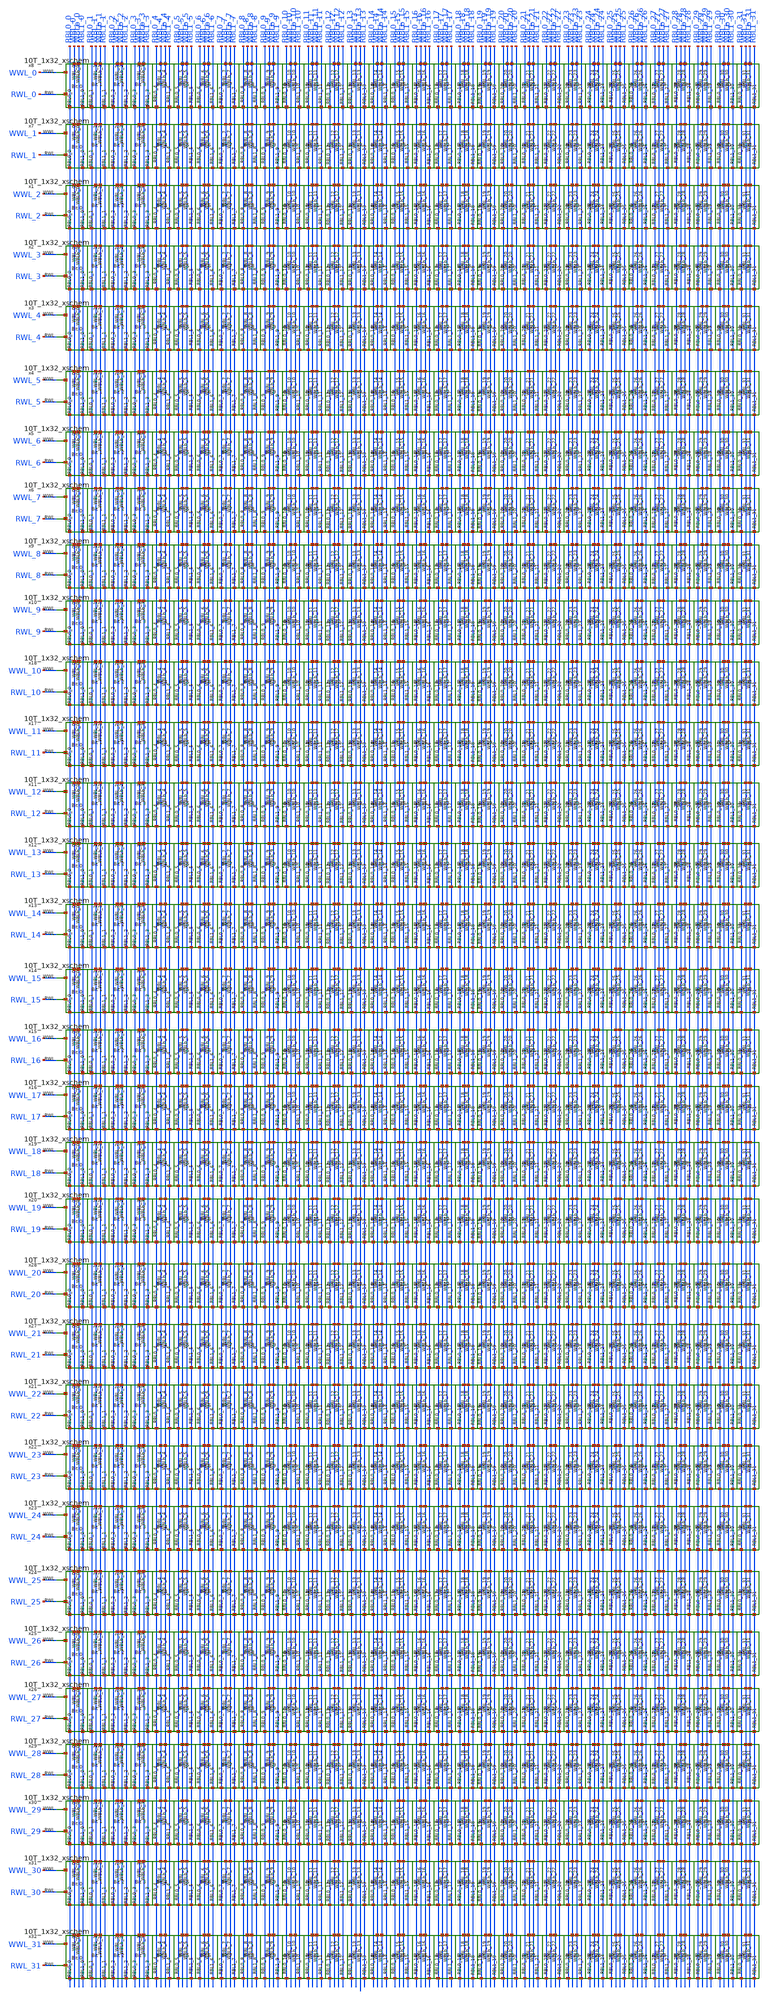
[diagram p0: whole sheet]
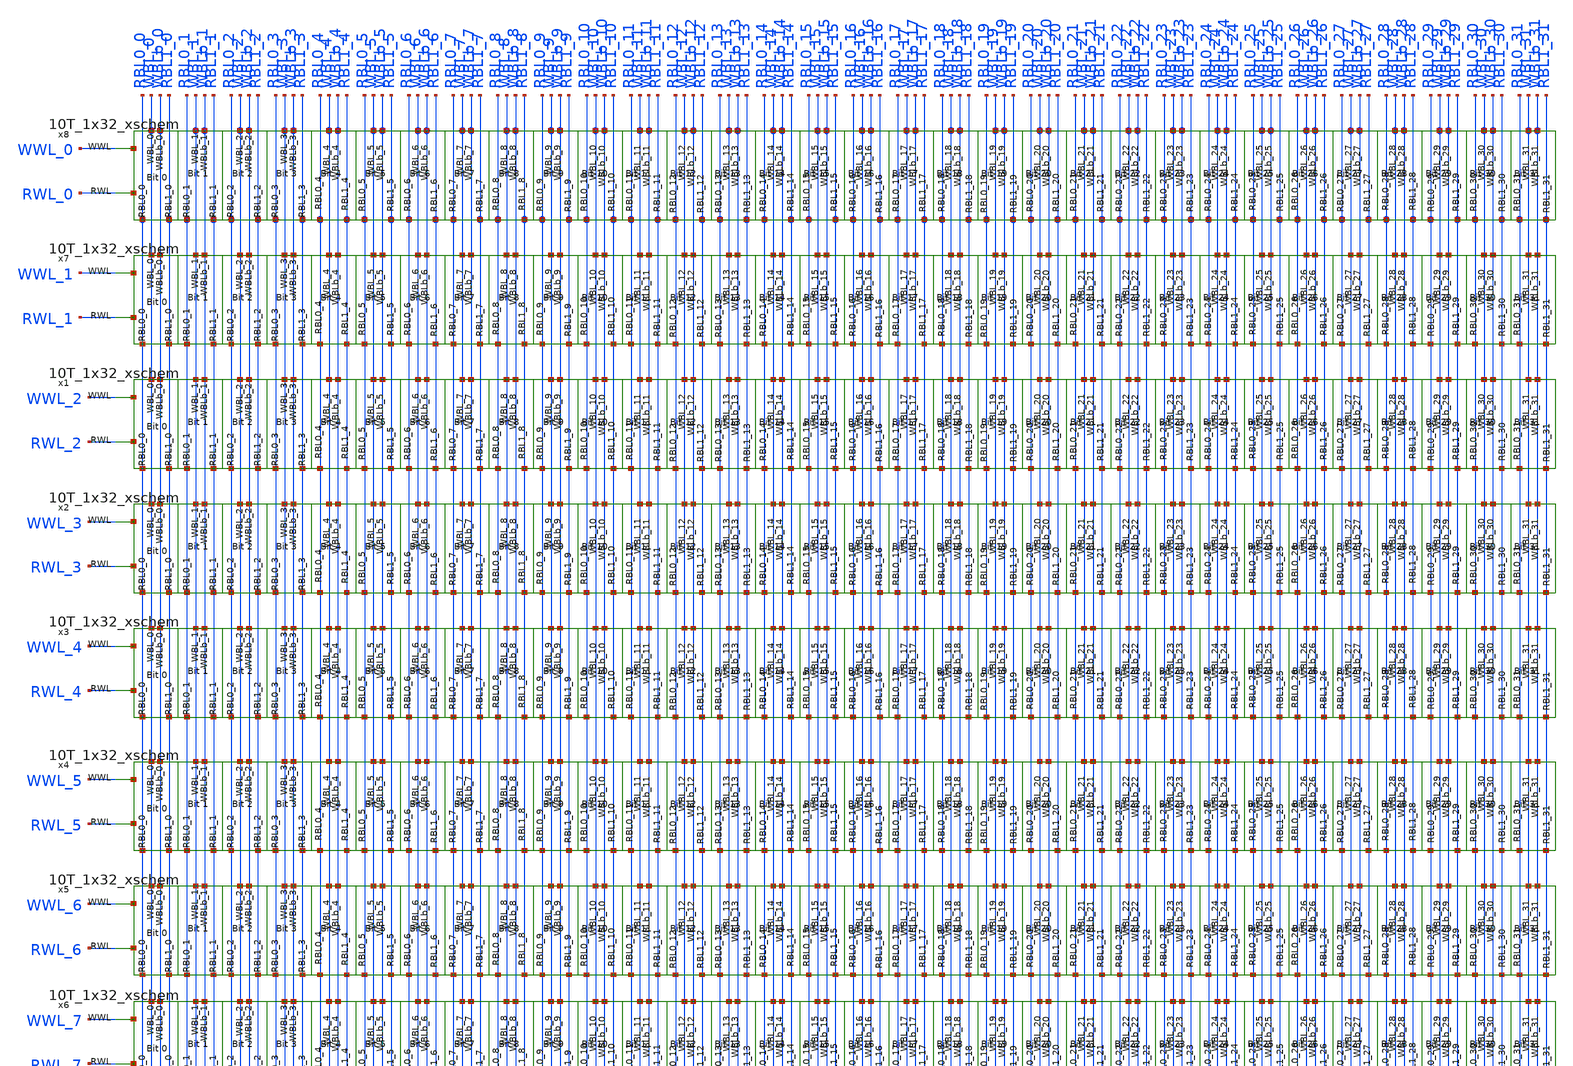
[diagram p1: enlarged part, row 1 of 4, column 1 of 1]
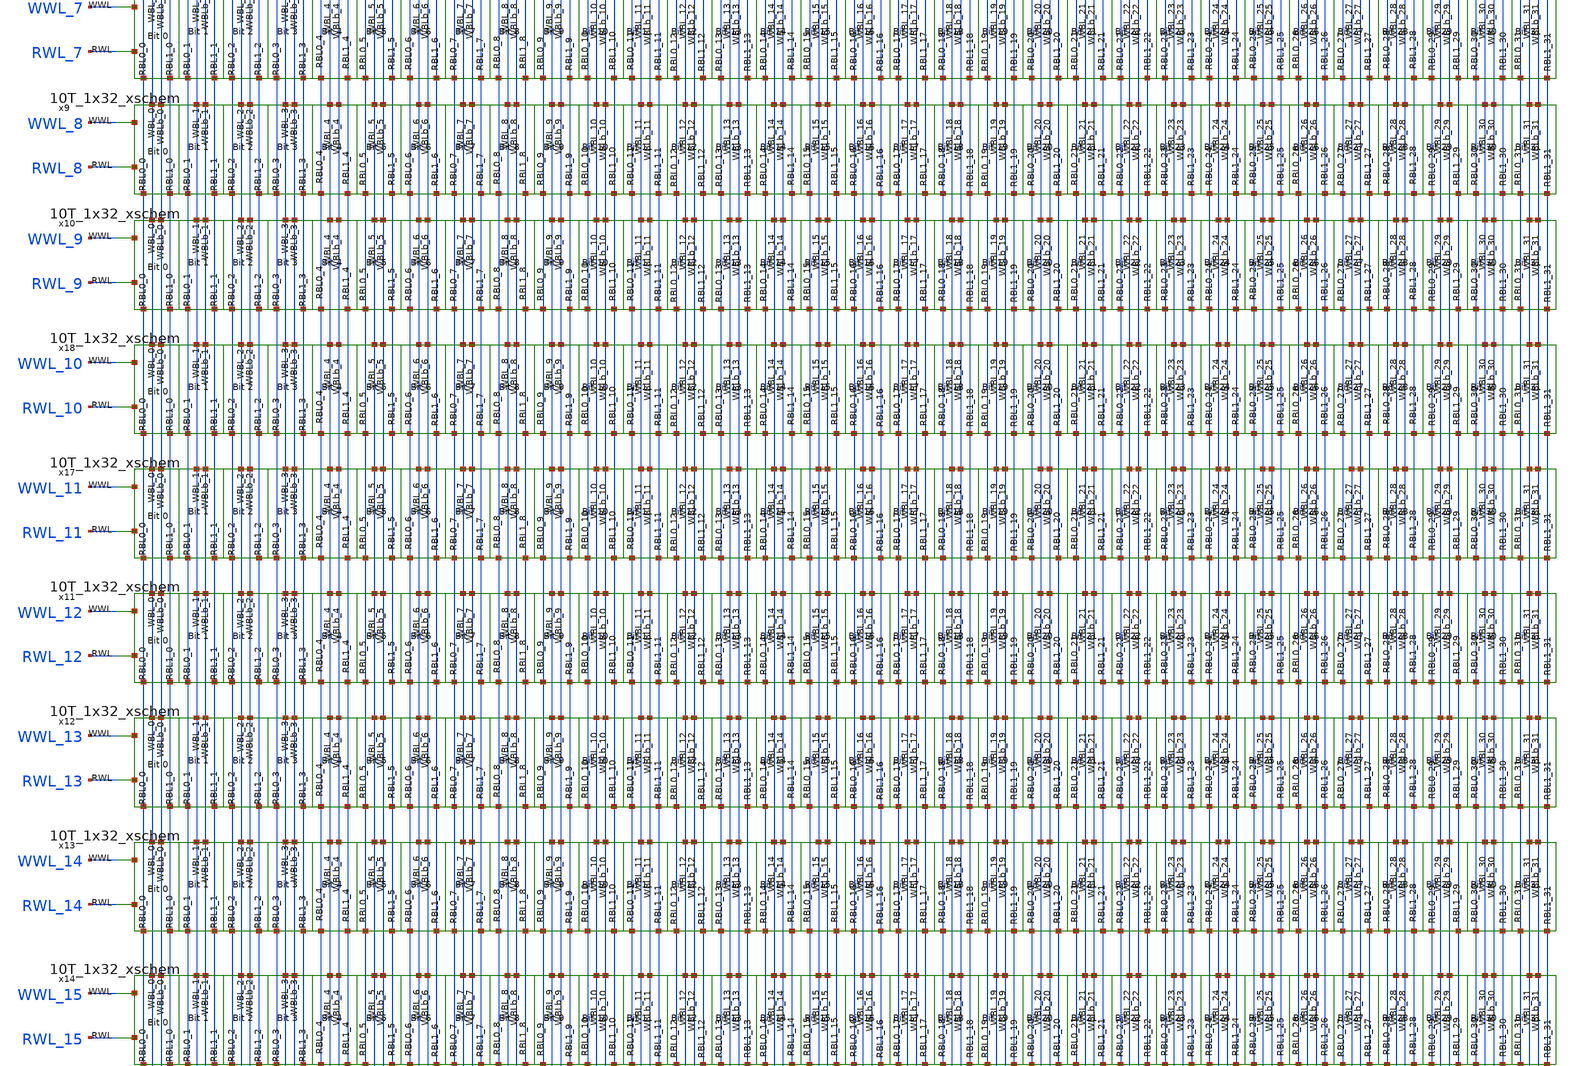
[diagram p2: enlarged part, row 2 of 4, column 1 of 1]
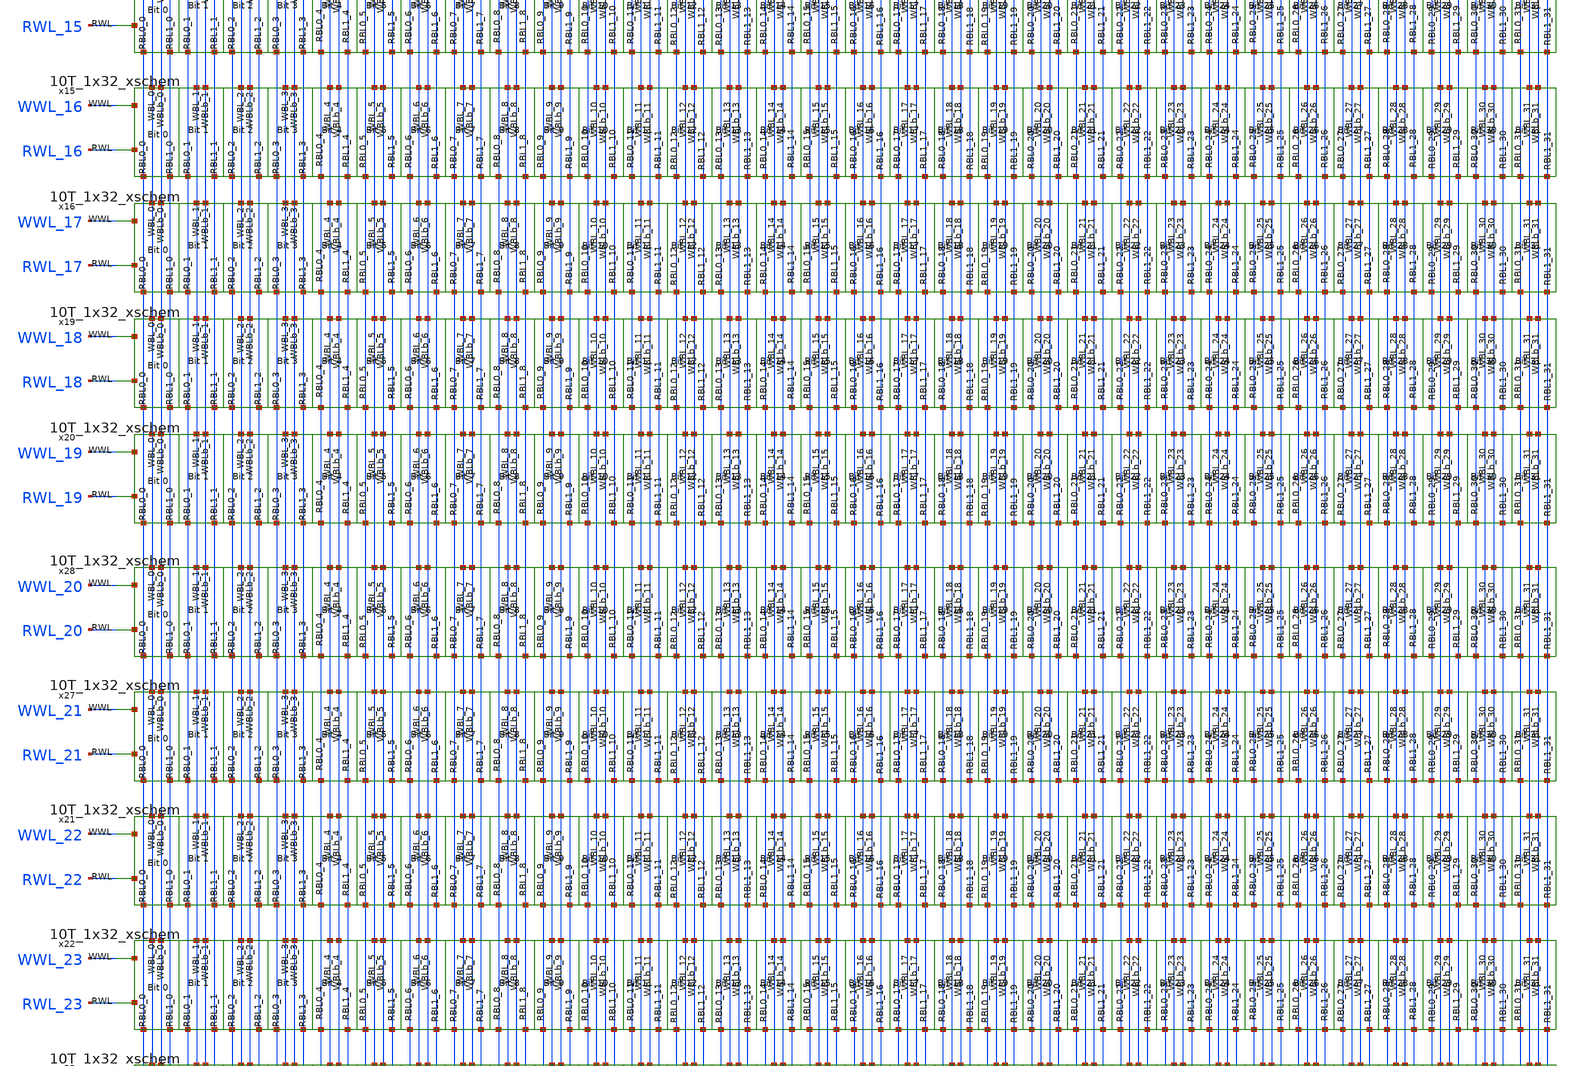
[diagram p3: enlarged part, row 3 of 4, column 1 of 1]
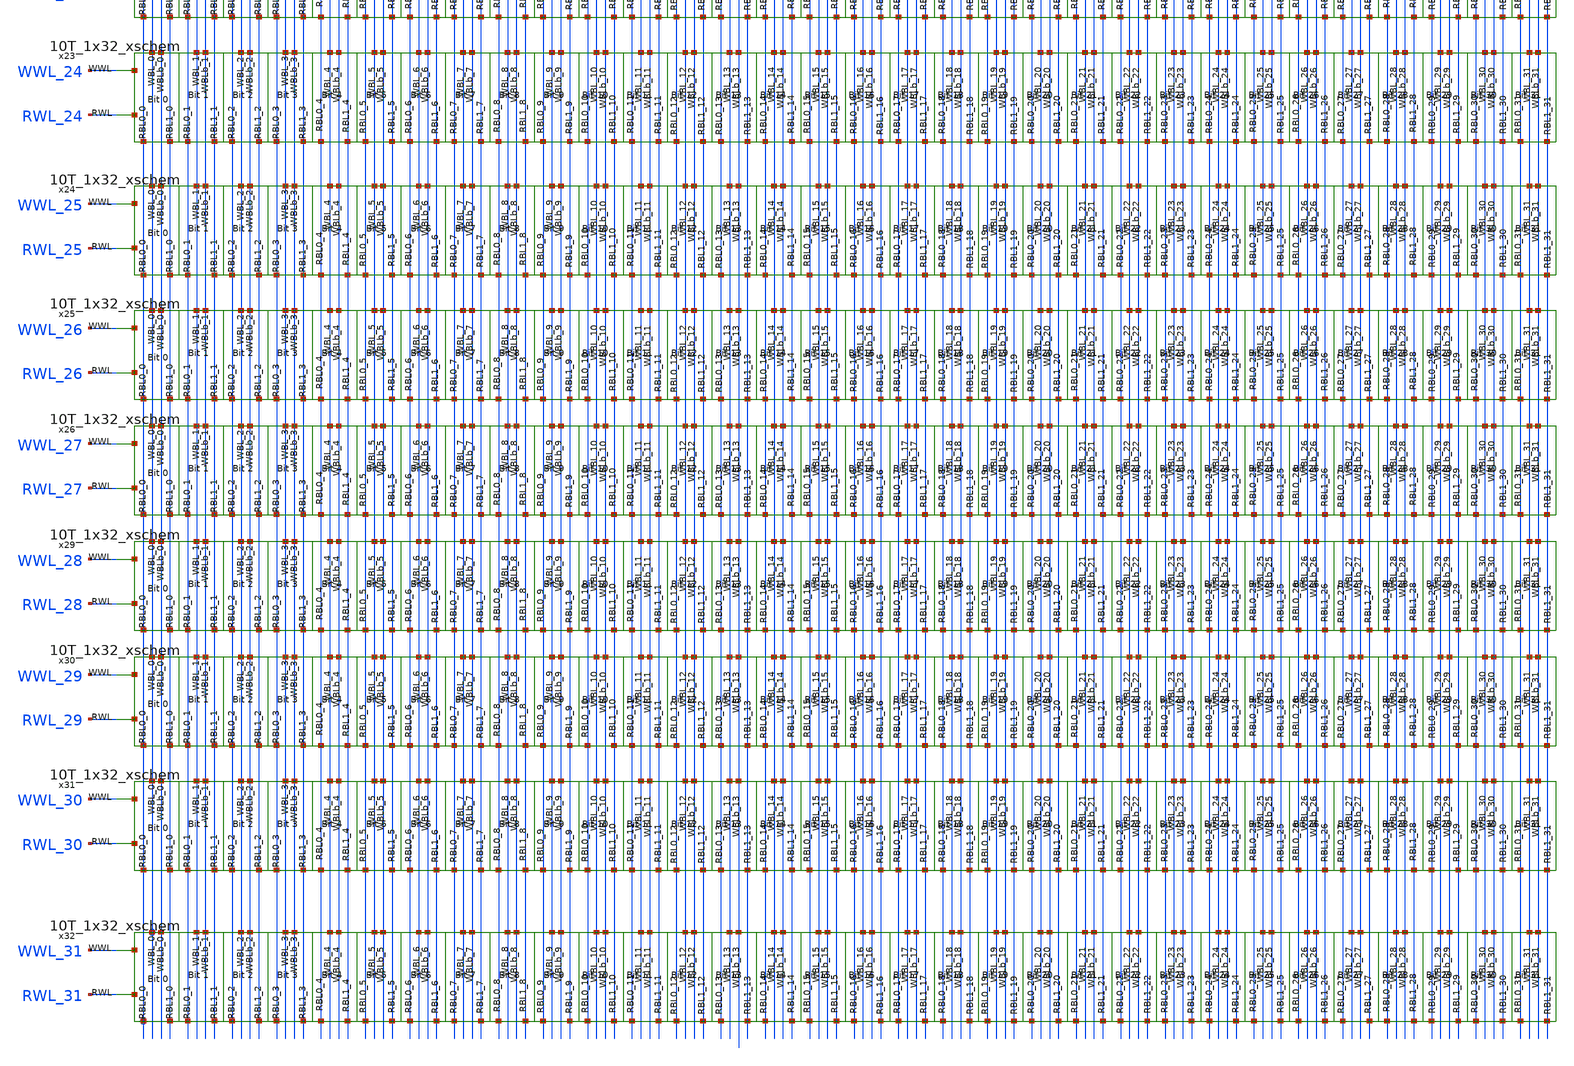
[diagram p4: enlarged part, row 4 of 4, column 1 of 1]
** sch_path: custom_layout/10T_32x32_xschem.sch
**.subckt 10T_32x32_xschem
x1 RBL0_22 WBL_25 RBL0_30 WBL_17 WBL_9 WBL_1 RBL0_14 RBL0_6 WBL_18 RBL0_18 RBL0_26 WBL_26 WBL_2
+ RBL0_2 RBL0_10 WBL_10 WBL_19 WBL_27 RBL1_30 RBL1_22 RBL1_14 WBL_3 RBL1_6 WBL_11 WBLb_30 WBLb_22 RBL0_31
+ RBL0_23 RBL0_7 RBL0_15 WBLb_6 WBLb_14 RBL1_21 WBL_20 RBL1_29 WBL_28 WBL_12 RBL1_13 RBL1_5 WBL_4 RBL1_20
+ WBL_23 WBL_31 RBL1_28 WBL_15 RBL1_4 RBL1_12 WBL_7 WBLb_29 WBLb_21 RBL1_19 RBL1_27 RBL1_3 WBLb_5 WBLb_13
+ RBL1_11 WBL_24 WBL_16 RBL1_18 RBL1_26 WBL_8 RBL1_2 RBL1_10 WBL_0 WBLb_26 RBL0_29 WBLb_18 RBL0_21 WBLb_10
+ RBL0_5 RBL0_13 WBLb_2 RBL1_25 WBLb_25 WBLb_17 RBL1_17 WBLb_9 RBL1_1 WBLb_1 RBL1_9 WBLb_24 WBLb_16 RBL1_23
+ RBL1_31 WBLb_0 WBLb_8 RBL1_7 RBL1_15 WBL_29 WBL_21 RBL0_17 RBL0_25 WBL_5 RBL0_1 WBL_13 RBL0_9 RBL0_28
+ WBLb_28 WBLb_20 RBL0_20 WBLb_12 WBLb_4 RBL0_4 RBL0_12 RBL0_27 WBL_30 WBL_22 RBL0_19 WBL_14 RBL0_11 WBL_6
+ RBL0_3 RBL1_24 WBLb_27 WBLb_19 RBL1_16 WBLb_11 RBL1_8 WBLb_3 RBL1_0 RBL0_24 WBLb_31 WBLb_23 RBL0_16 RBL0_8
+ WBLb_15 RBL0_0 WBLb_7 WWL_2 RWL_2 VDD GND 10T_1x32_xschem
x2 RBL0_22 WBL_25 RBL0_30 WBL_17 WBL_9 WBL_1 RBL0_14 RBL0_6 WBL_18 RBL0_18 RBL0_26 WBL_26 WBL_2
+ RBL0_2 RBL0_10 WBL_10 WBL_19 WBL_27 RBL1_30 RBL1_22 RBL1_14 WBL_3 RBL1_6 WBL_11 WBLb_30 WBLb_22 RBL0_31
+ RBL0_23 RBL0_7 RBL0_15 WBLb_6 WBLb_14 RBL1_21 WBL_20 RBL1_29 WBL_28 WBL_12 RBL1_13 RBL1_5 WBL_4 RBL1_20
+ WBL_23 WBL_31 RBL1_28 WBL_15 RBL1_4 RBL1_12 WBL_7 WBLb_29 WBLb_21 RBL1_19 RBL1_27 RBL1_3 WBLb_5 WBLb_13
+ RBL1_11 WBL_24 WBL_16 RBL1_18 RBL1_26 WBL_8 RBL1_2 RBL1_10 WBL_0 WBLb_26 RBL0_29 WBLb_18 RBL0_21 WBLb_10
+ RBL0_5 RBL0_13 WBLb_2 RBL1_25 WBLb_25 WBLb_17 RBL1_17 WBLb_9 RBL1_1 WBLb_1 RBL1_9 WBLb_24 WBLb_16 RBL1_23
+ RBL1_31 WBLb_0 WBLb_8 RBL1_7 RBL1_15 WBL_29 WBL_21 RBL0_17 RBL0_25 WBL_5 RBL0_1 WBL_13 RBL0_9 RBL0_28
+ WBLb_28 WBLb_20 RBL0_20 WBLb_12 WBLb_4 RBL0_4 RBL0_12 RBL0_27 WBL_30 WBL_22 RBL0_19 WBL_14 RBL0_11 WBL_6
+ RBL0_3 RBL1_24 WBLb_27 WBLb_19 RBL1_16 WBLb_11 RBL1_8 WBLb_3 RBL1_0 RBL0_24 WBLb_31 WBLb_23 RBL0_16 RBL0_8
+ WBLb_15 RBL0_0 WBLb_7 WWL_3 RWL_3 VDD GND 10T_1x32_xschem
x3 RBL0_22 WBL_25 RBL0_30 WBL_17 WBL_9 WBL_1 RBL0_14 RBL0_6 WBL_18 RBL0_18 RBL0_26 WBL_26 WBL_2
+ RBL0_2 RBL0_10 WBL_10 WBL_19 WBL_27 RBL1_30 RBL1_22 RBL1_14 WBL_3 RBL1_6 WBL_11 WBLb_30 WBLb_22 RBL0_31
+ RBL0_23 RBL0_7 RBL0_15 WBLb_6 WBLb_14 RBL1_21 WBL_20 RBL1_29 WBL_28 WBL_12 RBL1_13 RBL1_5 WBL_4 RBL1_20
+ WBL_23 WBL_31 RBL1_28 WBL_15 RBL1_4 RBL1_12 WBL_7 WBLb_29 WBLb_21 RBL1_19 RBL1_27 RBL1_3 WBLb_5 WBLb_13
+ RBL1_11 WBL_24 WBL_16 RBL1_18 RBL1_26 WBL_8 RBL1_2 RBL1_10 WBL_0 WBLb_26 RBL0_29 WBLb_18 RBL0_21 WBLb_10
+ RBL0_5 RBL0_13 WBLb_2 RBL1_25 WBLb_25 WBLb_17 RBL1_17 WBLb_9 RBL1_1 WBLb_1 RBL1_9 WBLb_24 WBLb_16 RBL1_23
+ RBL1_31 WBLb_0 WBLb_8 RBL1_7 RBL1_15 WBL_29 WBL_21 RBL0_17 RBL0_25 WBL_5 RBL0_1 WBL_13 RBL0_9 RBL0_28
+ WBLb_28 WBLb_20 RBL0_20 WBLb_12 WBLb_4 RBL0_4 RBL0_12 RBL0_27 WBL_30 WBL_22 RBL0_19 WBL_14 RBL0_11 WBL_6
+ RBL0_3 RBL1_24 WBLb_27 WBLb_19 RBL1_16 WBLb_11 RBL1_8 WBLb_3 RBL1_0 RBL0_24 WBLb_31 WBLb_23 RBL0_16 RBL0_8
+ WBLb_15 RBL0_0 WBLb_7 WWL_4 RWL_4 VDD GND 10T_1x32_xschem
x4 RBL0_22 WBL_25 RBL0_30 WBL_17 WBL_9 WBL_1 RBL0_14 RBL0_6 WBL_18 RBL0_18 RBL0_26 WBL_26 WBL_2
+ RBL0_2 RBL0_10 WBL_10 WBL_19 WBL_27 RBL1_30 RBL1_22 RBL1_14 WBL_3 RBL1_6 WBL_11 WBLb_30 WBLb_22 RBL0_31
+ RBL0_23 RBL0_7 RBL0_15 WBLb_6 WBLb_14 RBL1_21 WBL_20 RBL1_29 WBL_28 WBL_12 RBL1_13 RBL1_5 WBL_4 RBL1_20
+ WBL_23 WBL_31 RBL1_28 WBL_15 RBL1_4 RBL1_12 WBL_7 WBLb_29 WBLb_21 RBL1_19 RBL1_27 RBL1_3 WBLb_5 WBLb_13
+ RBL1_11 WBL_24 WBL_16 RBL1_18 RBL1_26 WBL_8 RBL1_2 RBL1_10 WBL_0 WBLb_26 RBL0_29 WBLb_18 RBL0_21 WBLb_10
+ RBL0_5 RBL0_13 WBLb_2 RBL1_25 WBLb_25 WBLb_17 RBL1_17 WBLb_9 RBL1_1 WBLb_1 RBL1_9 WBLb_24 WBLb_16 RBL1_23
+ RBL1_31 WBLb_0 WBLb_8 RBL1_7 RBL1_15 WBL_29 WBL_21 RBL0_17 RBL0_25 WBL_5 RBL0_1 WBL_13 RBL0_9 RBL0_28
+ WBLb_28 WBLb_20 RBL0_20 WBLb_12 WBLb_4 RBL0_4 RBL0_12 RBL0_27 WBL_30 WBL_22 RBL0_19 WBL_14 RBL0_11 WBL_6
+ RBL0_3 RBL1_24 WBLb_27 WBLb_19 RBL1_16 WBLb_11 RBL1_8 WBLb_3 RBL1_0 RBL0_24 WBLb_31 WBLb_23 RBL0_16 RBL0_8
+ WBLb_15 RBL0_0 WBLb_7 WWL_5 RWL_5 VDD GND 10T_1x32_xschem
x5 RBL0_22 WBL_25 RBL0_30 WBL_17 WBL_9 WBL_1 RBL0_14 RBL0_6 WBL_18 RBL0_18 RBL0_26 WBL_26 WBL_2
+ RBL0_2 RBL0_10 WBL_10 WBL_19 WBL_27 RBL1_30 RBL1_22 RBL1_14 WBL_3 RBL1_6 WBL_11 WBLb_30 WBLb_22 RBL0_31
+ RBL0_23 RBL0_7 RBL0_15 WBLb_6 WBLb_14 RBL1_21 WBL_20 RBL1_29 WBL_28 WBL_12 RBL1_13 RBL1_5 WBL_4 RBL1_20
+ WBL_23 WBL_31 RBL1_28 WBL_15 RBL1_4 RBL1_12 WBL_7 WBLb_29 WBLb_21 RBL1_19 RBL1_27 RBL1_3 WBLb_5 WBLb_13
+ RBL1_11 WBL_24 WBL_16 RBL1_18 RBL1_26 WBL_8 RBL1_2 RBL1_10 WBL_0 WBLb_26 RBL0_29 WBLb_18 RBL0_21 WBLb_10
+ RBL0_5 RBL0_13 WBLb_2 RBL1_25 WBLb_25 WBLb_17 RBL1_17 WBLb_9 RBL1_1 WBLb_1 RBL1_9 WBLb_24 WBLb_16 RBL1_23
+ RBL1_31 WBLb_0 WBLb_8 RBL1_7 RBL1_15 WBL_29 WBL_21 RBL0_17 RBL0_25 WBL_5 RBL0_1 WBL_13 RBL0_9 RBL0_28
+ WBLb_28 WBLb_20 RBL0_20 WBLb_12 WBLb_4 RBL0_4 RBL0_12 RBL0_27 WBL_30 WBL_22 RBL0_19 WBL_14 RBL0_11 WBL_6
+ RBL0_3 RBL1_24 WBLb_27 WBLb_19 RBL1_16 WBLb_11 RBL1_8 WBLb_3 RBL1_0 RBL0_24 WBLb_31 WBLb_23 RBL0_16 RBL0_8
+ WBLb_15 RBL0_0 WBLb_7 WWL_6 RWL_6 VDD GND 10T_1x32_xschem
x6 RBL0_22 WBL_25 RBL0_30 WBL_17 WBL_9 WBL_1 RBL0_14 RBL0_6 WBL_18 RBL0_18 RBL0_26 WBL_26 WBL_2
+ RBL0_2 RBL0_10 WBL_10 WBL_19 WBL_27 RBL1_30 RBL1_22 RBL1_14 WBL_3 RBL1_6 WBL_11 WBLb_30 WBLb_22 RBL0_31
+ RBL0_23 RBL0_7 RBL0_15 WBLb_6 WBLb_14 RBL1_21 WBL_20 RBL1_29 WBL_28 WBL_12 RBL1_13 RBL1_5 WBL_4 RBL1_20
+ WBL_23 WBL_31 RBL1_28 WBL_15 RBL1_4 RBL1_12 WBL_7 WBLb_29 WBLb_21 RBL1_19 RBL1_27 RBL1_3 WBLb_5 WBLb_13
+ RBL1_11 WBL_24 WBL_16 RBL1_18 RBL1_26 WBL_8 RBL1_2 RBL1_10 WBL_0 WBLb_26 RBL0_29 WBLb_18 RBL0_21 WBLb_10
+ RBL0_5 RBL0_13 WBLb_2 RBL1_25 WBLb_25 WBLb_17 RBL1_17 WBLb_9 RBL1_1 WBLb_1 RBL1_9 WBLb_24 WBLb_16 RBL1_23
+ RBL1_31 WBLb_0 WBLb_8 RBL1_7 RBL1_15 WBL_29 WBL_21 RBL0_17 RBL0_25 WBL_5 RBL0_1 WBL_13 RBL0_9 RBL0_28
+ WBLb_28 WBLb_20 RBL0_20 WBLb_12 WBLb_4 RBL0_4 RBL0_12 RBL0_27 WBL_30 WBL_22 RBL0_19 WBL_14 RBL0_11 WBL_6
+ RBL0_3 RBL1_24 WBLb_27 WBLb_19 RBL1_16 WBLb_11 RBL1_8 WBLb_3 RBL1_0 RBL0_24 WBLb_31 WBLb_23 RBL0_16 RBL0_8
+ WBLb_15 RBL0_0 WBLb_7 net1 RWL_7 VDD GND 10T_1x32_xschem
x7 RBL0_22 WBL_25 RBL0_30 WBL_17 WBL_9 WBL_1 RBL0_14 RBL0_6 WBL_18 RBL0_18 RBL0_26 WBL_26 WBL_2
+ RBL0_2 RBL0_10 WBL_10 WBL_19 WBL_27 RBL1_30 RBL1_22 RBL1_14 WBL_3 RBL1_6 WBL_11 WBLb_30 WBLb_22 RBL0_31
+ RBL0_23 RBL0_7 RBL0_15 WBLb_6 WBLb_14 RBL1_21 WBL_20 RBL1_29 WBL_28 WBL_12 RBL1_13 RBL1_5 WBL_4 RBL1_20
+ WBL_23 WBL_31 RBL1_28 WBL_15 RBL1_4 RBL1_12 WBL_7 WBLb_29 WBLb_21 RBL1_19 RBL1_27 RBL1_3 WBLb_5 WBLb_13
+ RBL1_11 WBL_24 WBL_16 RBL1_18 RBL1_26 WBL_8 RBL1_2 RBL1_10 WBL_0 WBLb_26 RBL0_29 WBLb_18 RBL0_21 WBLb_10
+ RBL0_5 RBL0_13 WBLb_2 RBL1_25 WBLb_25 WBLb_17 RBL1_17 WBLb_9 RBL1_1 WBLb_1 RBL1_9 WBLb_24 WBLb_16 RBL1_23
+ RBL1_31 WBLb_0 WBLb_8 RBL1_7 RBL1_15 WBL_29 WBL_21 RBL0_17 RBL0_25 WBL_5 RBL0_1 WBL_13 RBL0_9 RBL0_28
+ WBLb_28 WBLb_20 RBL0_20 WBLb_12 WBLb_4 RBL0_4 RBL0_12 RBL0_27 WBL_30 WBL_22 RBL0_19 WBL_14 RBL0_11 WBL_6
+ RBL0_3 RBL1_24 WBLb_27 WBLb_19 RBL1_16 WBLb_11 RBL1_8 WBLb_3 RBL1_0 RBL0_24 WBLb_31 WBLb_23 RBL0_16 RBL0_8
+ WBLb_15 RBL0_0 WBLb_7 WWL_1 RWL_1 VDD GND 10T_1x32_xschem
x8 RBL0_22 WBL_25 RBL0_30 WBL_17 WBL_9 WBL_1 RBL0_14 RBL0_6 WBL_18 RBL0_18 RBL0_26 WBL_26 WBL_2
+ RBL0_2 RBL0_10 WBL_10 WBL_19 WBL_27 RBL1_30 RBL1_22 RBL1_14 WBL_3 RBL1_6 WBL_11 WBLb_30 WBLb_22 RBL0_31
+ RBL0_23 RBL0_7 RBL0_15 WBLb_6 WBLb_14 RBL1_21 WBL_20 RBL1_29 WBL_28 WBL_12 RBL1_13 RBL1_5 WBL_4 RBL1_20
+ WBL_23 WBL_31 RBL1_28 WBL_15 RBL1_4 RBL1_12 WBL_7 WBLb_29 WBLb_21 RBL1_19 RBL1_27 RBL1_3 WBLb_5 WBLb_13
+ RBL1_11 WBL_24 WBL_16 RBL1_18 RBL1_26 WBL_8 RBL1_2 RBL1_10 WBL_0 WBLb_26 RBL0_29 WBLb_18 RBL0_21 WBLb_10
+ RBL0_5 RBL0_13 WBLb_2 RBL1_25 WBLb_25 WBLb_17 RBL1_17 WBLb_9 RBL1_1 WBLb_1 RBL1_9 WBLb_24 WBLb_16 RBL1_23
+ RBL1_31 WBLb_0 WBLb_8 RBL1_7 RBL1_15 WBL_29 WBL_21 RBL0_17 RBL0_25 WBL_5 RBL0_1 WBL_13 RBL0_9 RBL0_28
+ WBLb_28 WBLb_20 RBL0_20 WBLb_12 WBLb_4 RBL0_4 RBL0_12 RBL0_27 WBL_30 WBL_22 RBL0_19 WBL_14 RBL0_11 WBL_6
+ RBL0_3 RBL1_24 WBLb_27 WBLb_19 RBL1_16 WBLb_11 RBL1_8 WBLb_3 RBL1_0 RBL0_24 WBLb_31 WBLb_23 RBL0_16 RBL0_8
+ WBLb_15 RBL0_0 WBLb_7 WWL_0 RWL_0 VDD GND 10T_1x32_xschem
x9 RBL0_22 WBL_25 RBL0_30 WBL_17 WBL_9 WBL_1 RBL0_14 RBL0_6 WBL_18 RBL0_18 RBL0_26 WBL_26 WBL_2
+ RBL0_2 RBL0_10 WBL_10 WBL_19 WBL_27 RBL1_30 RBL1_22 RBL1_14 WBL_3 RBL1_6 WBL_11 WBLb_30 WBLb_22 RBL0_31
+ RBL0_23 RBL0_7 RBL0_15 WBLb_6 WBLb_14 RBL1_21 WBL_20 RBL1_29 WBL_28 WBL_12 RBL1_13 RBL1_5 WBL_4 RBL1_20
+ WBL_23 WBL_31 RBL1_28 WBL_15 RBL1_4 RBL1_12 WBL_7 WBLb_29 WBLb_21 RBL1_19 RBL1_27 RBL1_3 WBLb_5 WBLb_13
+ RBL1_11 WBL_24 WBL_16 RBL1_18 RBL1_26 WBL_8 RBL1_2 RBL1_10 WBL_0 WBLb_26 RBL0_29 WBLb_18 RBL0_21 WBLb_10
+ RBL0_5 RBL0_13 WBLb_2 RBL1_25 WBLb_25 WBLb_17 RBL1_17 WBLb_9 RBL1_1 WBLb_1 RBL1_9 WBLb_24 WBLb_16 RBL1_23
+ RBL1_31 WBLb_0 WBLb_8 RBL1_7 RBL1_15 WBL_29 WBL_21 RBL0_17 RBL0_25 WBL_5 RBL0_1 WBL_13 RBL0_9 RBL0_28
+ WBLb_28 WBLb_20 RBL0_20 WBLb_12 WBLb_4 RBL0_4 RBL0_12 RBL0_27 WBL_30 WBL_22 RBL0_19 WBL_14 RBL0_11 WBL_6
+ RBL0_3 RBL1_24 WBLb_27 WBLb_19 RBL1_16 WBLb_11 RBL1_8 WBLb_3 RBL1_0 RBL0_24 WBLb_31 WBLb_23 RBL0_16 RBL0_8
+ WBLb_15 RBL0_0 WBLb_7 WWL_8 RWL_8 VDD GND 10T_1x32_xschem
x10 RBL0_22 WBL_25 RBL0_30 WBL_17 WBL_9 WBL_1 RBL0_14 RBL0_6 WBL_18 RBL0_18 RBL0_26 WBL_26 WBL_2
+ RBL0_2 RBL0_10 WBL_10 WBL_19 WBL_27 RBL1_30 RBL1_22 RBL1_14 WBL_3 RBL1_6 WBL_11 WBLb_30 WBLb_22 RBL0_31
+ RBL0_23 RBL0_7 RBL0_15 WBLb_6 WBLb_14 RBL1_21 WBL_20 RBL1_29 WBL_28 WBL_12 RBL1_13 RBL1_5 WBL_4 RBL1_20
+ WBL_23 WBL_31 RBL1_28 WBL_15 RBL1_4 RBL1_12 WBL_7 WBLb_29 WBLb_21 RBL1_19 RBL1_27 RBL1_3 WBLb_5 WBLb_13
+ RBL1_11 WBL_24 WBL_16 RBL1_18 RBL1_26 WBL_8 RBL1_2 RBL1_10 WBL_0 WBLb_26 RBL0_29 WBLb_18 RBL0_21 WBLb_10
+ RBL0_5 RBL0_13 WBLb_2 RBL1_25 WBLb_25 WBLb_17 RBL1_17 WBLb_9 RBL1_1 WBLb_1 RBL1_9 WBLb_24 WBLb_16 RBL1_23
+ RBL1_31 WBLb_0 WBLb_8 RBL1_7 RBL1_15 WBL_29 WBL_21 RBL0_17 RBL0_25 WBL_5 RBL0_1 WBL_13 RBL0_9 RBL0_28
+ WBLb_28 WBLb_20 RBL0_20 WBLb_12 WBLb_4 RBL0_4 RBL0_12 RBL0_27 WBL_30 WBL_22 RBL0_19 WBL_14 RBL0_11 WBL_6
+ RBL0_3 RBL1_24 WBLb_27 WBLb_19 RBL1_16 WBLb_11 RBL1_8 WBLb_3 RBL1_0 RBL0_24 WBLb_31 WBLb_23 RBL0_16 RBL0_8
+ WBLb_15 RBL0_0 WBLb_7 WWL_9 RWL_9 VDD GND 10T_1x32_xschem
x11 RBL0_22 WBL_25 RBL0_30 WBL_17 WBL_9 WBL_1 RBL0_14 RBL0_6 WBL_18 RBL0_18 RBL0_26 WBL_26 WBL_2
+ RBL0_2 RBL0_10 WBL_10 WBL_19 WBL_27 RBL1_30 RBL1_22 RBL1_14 WBL_3 RBL1_6 WBL_11 WBLb_30 WBLb_22 RBL0_31
+ RBL0_23 RBL0_7 RBL0_15 WBLb_6 WBLb_14 RBL1_21 WBL_20 RBL1_29 WBL_28 WBL_12 RBL1_13 RBL1_5 WBL_4 RBL1_20
+ WBL_23 WBL_31 RBL1_28 WBL_15 RBL1_4 RBL1_12 WBL_7 WBLb_29 WBLb_21 RBL1_19 RBL1_27 RBL1_3 WBLb_5 WBLb_13
+ RBL1_11 WBL_24 WBL_16 RBL1_18 RBL1_26 WBL_8 RBL1_2 RBL1_10 WBL_0 WBLb_26 RBL0_29 WBLb_18 RBL0_21 WBLb_10
+ RBL0_5 RBL0_13 WBLb_2 RBL1_25 WBLb_25 WBLb_17 RBL1_17 WBLb_9 RBL1_1 WBLb_1 RBL1_9 WBLb_24 WBLb_16 RBL1_23
+ RBL1_31 WBLb_0 WBLb_8 RBL1_7 RBL1_15 WBL_29 WBL_21 RBL0_17 RBL0_25 WBL_5 RBL0_1 WBL_13 RBL0_9 RBL0_28
+ WBLb_28 WBLb_20 RBL0_20 WBLb_12 WBLb_4 RBL0_4 RBL0_12 RBL0_27 WBL_30 WBL_22 RBL0_19 WBL_14 RBL0_11 WBL_6
+ RBL0_3 RBL1_24 WBLb_27 WBLb_19 RBL1_16 WBLb_11 RBL1_8 WBLb_3 RBL1_0 RBL0_24 WBLb_31 WBLb_23 RBL0_16 RBL0_8
+ WBLb_15 RBL0_0 WBLb_7 WWL_12 RWL_12 VDD GND 10T_1x32_xschem
x12 RBL0_22 WBL_25 RBL0_30 WBL_17 WBL_9 WBL_1 RBL0_14 RBL0_6 WBL_18 RBL0_18 RBL0_26 WBL_26 WBL_2
+ RBL0_2 RBL0_10 WBL_10 WBL_19 WBL_27 RBL1_30 RBL1_22 RBL1_14 WBL_3 RBL1_6 WBL_11 WBLb_30 WBLb_22 RBL0_31
+ RBL0_23 RBL0_7 RBL0_15 WBLb_6 WBLb_14 RBL1_21 WBL_20 RBL1_29 WBL_28 WBL_12 RBL1_13 RBL1_5 WBL_4 RBL1_20
+ WBL_23 WBL_31 RBL1_28 WBL_15 RBL1_4 RBL1_12 WBL_7 WBLb_29 WBLb_21 RBL1_19 RBL1_27 RBL1_3 WBLb_5 WBLb_13
+ RBL1_11 WBL_24 WBL_16 RBL1_18 RBL1_26 WBL_8 RBL1_2 RBL1_10 WBL_0 WBLb_26 RBL0_29 WBLb_18 RBL0_21 WBLb_10
+ RBL0_5 RBL0_13 WBLb_2 RBL1_25 WBLb_25 WBLb_17 RBL1_17 WBLb_9 RBL1_1 WBLb_1 RBL1_9 WBLb_24 WBLb_16 RBL1_23
+ RBL1_31 WBLb_0 WBLb_8 RBL1_7 RBL1_15 WBL_29 WBL_21 RBL0_17 RBL0_25 WBL_5 RBL0_1 WBL_13 RBL0_9 RBL0_28
+ WBLb_28 WBLb_20 RBL0_20 WBLb_12 WBLb_4 RBL0_4 RBL0_12 RBL0_27 WBL_30 WBL_22 RBL0_19 WBL_14 RBL0_11 WBL_6
+ RBL0_3 RBL1_24 WBLb_27 WBLb_19 RBL1_16 WBLb_11 RBL1_8 WBLb_3 RBL1_0 RBL0_24 WBLb_31 WBLb_23 RBL0_16 RBL0_8
+ WBLb_15 RBL0_0 WBLb_7 WWL_13 RWL_13 VDD GND 10T_1x32_xschem
x13 RBL0_22 WBL_25 RBL0_30 WBL_17 WBL_9 WBL_1 RBL0_14 RBL0_6 WBL_18 RBL0_18 RBL0_26 WBL_26 WBL_2
+ RBL0_2 RBL0_10 WBL_10 WBL_19 WBL_27 RBL1_30 RBL1_22 RBL1_14 WBL_3 RBL1_6 WBL_11 WBLb_30 WBLb_22 RBL0_31
+ RBL0_23 RBL0_7 RBL0_15 WBLb_6 WBLb_14 RBL1_21 WBL_20 RBL1_29 WBL_28 WBL_12 RBL1_13 RBL1_5 WBL_4 RBL1_20
+ WBL_23 WBL_31 RBL1_28 WBL_15 RBL1_4 RBL1_12 WBL_7 WBLb_29 WBLb_21 RBL1_19 RBL1_27 RBL1_3 WBLb_5 WBLb_13
+ RBL1_11 WBL_24 WBL_16 RBL1_18 RBL1_26 WBL_8 RBL1_2 RBL1_10 WBL_0 WBLb_26 RBL0_29 WBLb_18 RBL0_21 WBLb_10
+ RBL0_5 RBL0_13 WBLb_2 RBL1_25 WBLb_25 WBLb_17 RBL1_17 WBLb_9 RBL1_1 WBLb_1 RBL1_9 WBLb_24 WBLb_16 RBL1_23
+ RBL1_31 WBLb_0 WBLb_8 RBL1_7 RBL1_15 WBL_29 WBL_21 RBL0_17 RBL0_25 WBL_5 RBL0_1 WBL_13 RBL0_9 RBL0_28
+ WBLb_28 WBLb_20 RBL0_20 WBLb_12 WBLb_4 RBL0_4 RBL0_12 RBL0_27 WBL_30 WBL_22 RBL0_19 WBL_14 RBL0_11 WBL_6
+ RBL0_3 RBL1_24 WBLb_27 WBLb_19 RBL1_16 WBLb_11 RBL1_8 WBLb_3 RBL1_0 RBL0_24 WBLb_31 WBLb_23 RBL0_16 RBL0_8
+ WBLb_15 RBL0_0 WBLb_7 WWL_14 RWL_14 VDD GND 10T_1x32_xschem
x14 RBL0_22 WBL_25 RBL0_30 WBL_17 WBL_9 WBL_1 RBL0_14 RBL0_6 WBL_18 RBL0_18 RBL0_26 WBL_26 WBL_2
+ RBL0_2 RBL0_10 WBL_10 WBL_19 WBL_27 RBL1_30 RBL1_22 RBL1_14 WBL_3 RBL1_6 WBL_11 WBLb_30 WBLb_22 RBL0_31
+ RBL0_23 RBL0_7 RBL0_15 WBLb_6 WBLb_14 RBL1_21 WBL_20 RBL1_29 WBL_28 WBL_12 RBL1_13 RBL1_5 WBL_4 RBL1_20
+ WBL_23 WBL_31 RBL1_28 WBL_15 RBL1_4 RBL1_12 WBL_7 WBLb_29 WBLb_21 RBL1_19 RBL1_27 RBL1_3 WBLb_5 WBLb_13
+ RBL1_11 WBL_24 WBL_16 RBL1_18 RBL1_26 WBL_8 RBL1_2 RBL1_10 WBL_0 WBLb_26 RBL0_29 WBLb_18 RBL0_21 WBLb_10
+ RBL0_5 RBL0_13 WBLb_2 RBL1_25 WBLb_25 WBLb_17 RBL1_17 WBLb_9 RBL1_1 WBLb_1 RBL1_9 WBLb_24 WBLb_16 RBL1_23
+ RBL1_31 WBLb_0 WBLb_8 RBL1_7 RBL1_15 WBL_29 WBL_21 RBL0_17 RBL0_25 WBL_5 RBL0_1 WBL_13 RBL0_9 RBL0_28
+ WBLb_28 WBLb_20 RBL0_20 WBLb_12 WBLb_4 RBL0_4 RBL0_12 RBL0_27 WBL_30 WBL_22 RBL0_19 WBL_14 RBL0_11 WBL_6
+ RBL0_3 RBL1_24 WBLb_27 WBLb_19 RBL1_16 WBLb_11 RBL1_8 WBLb_3 RBL1_0 RBL0_24 WBLb_31 WBLb_23 RBL0_16 RBL0_8
+ WBLb_15 RBL0_0 WBLb_7 WWL_15 RWL_15 VDD GND 10T_1x32_xschem
x15 RBL0_22 WBL_25 RBL0_30 WBL_17 WBL_9 WBL_1 RBL0_14 RBL0_6 WBL_18 RBL0_18 RBL0_26 WBL_26 WBL_2
+ RBL0_2 RBL0_10 WBL_10 WBL_19 WBL_27 RBL1_30 RBL1_22 RBL1_14 WBL_3 RBL1_6 WBL_11 WBLb_30 WBLb_22 RBL0_31
+ RBL0_23 RBL0_7 RBL0_15 WBLb_6 WBLb_14 RBL1_21 WBL_20 RBL1_29 WBL_28 WBL_12 RBL1_13 RBL1_5 WBL_4 RBL1_20
+ WBL_23 WBL_31 RBL1_28 WBL_15 RBL1_4 RBL1_12 WBL_7 WBLb_29 WBLb_21 RBL1_19 RBL1_27 RBL1_3 WBLb_5 WBLb_13
+ RBL1_11 WBL_24 WBL_16 RBL1_18 RBL1_26 WBL_8 RBL1_2 RBL1_10 WBL_0 WBLb_26 RBL0_29 WBLb_18 RBL0_21 WBLb_10
+ RBL0_5 RBL0_13 WBLb_2 RBL1_25 WBLb_25 WBLb_17 RBL1_17 WBLb_9 RBL1_1 WBLb_1 RBL1_9 WBLb_24 WBLb_16 RBL1_23
+ RBL1_31 WBLb_0 WBLb_8 RBL1_7 RBL1_15 WBL_29 WBL_21 RBL0_17 RBL0_25 WBL_5 RBL0_1 WBL_13 RBL0_9 RBL0_28
+ WBLb_28 WBLb_20 RBL0_20 WBLb_12 WBLb_4 RBL0_4 RBL0_12 RBL0_27 WBL_30 WBL_22 RBL0_19 WBL_14 RBL0_11 WBL_6
+ RBL0_3 RBL1_24 WBLb_27 WBLb_19 RBL1_16 WBLb_11 RBL1_8 WBLb_3 RBL1_0 RBL0_24 WBLb_31 WBLb_23 RBL0_16 RBL0_8
+ WBLb_15 RBL0_0 WBLb_7 WWL_16 RWL_16 VDD GND 10T_1x32_xschem
x16 RBL0_22 WBL_25 RBL0_30 WBL_17 WBL_9 WBL_1 RBL0_14 RBL0_6 WBL_18 RBL0_18 RBL0_26 WBL_26 WBL_2
+ RBL0_2 RBL0_10 WBL_10 WBL_19 WBL_27 RBL1_30 RBL1_22 RBL1_14 WBL_3 RBL1_6 WBL_11 WBLb_30 WBLb_22 RBL0_31
+ RBL0_23 RBL0_7 RBL0_15 WBLb_6 WBLb_14 RBL1_21 WBL_20 RBL1_29 WBL_28 WBL_12 RBL1_13 RBL1_5 WBL_4 RBL1_20
+ WBL_23 WBL_31 RBL1_28 WBL_15 RBL1_4 RBL1_12 WBL_7 WBLb_29 WBLb_21 RBL1_19 RBL1_27 RBL1_3 WBLb_5 WBLb_13
+ RBL1_11 WBL_24 WBL_16 RBL1_18 RBL1_26 WBL_8 RBL1_2 RBL1_10 WBL_0 WBLb_26 RBL0_29 WBLb_18 RBL0_21 WBLb_10
+ RBL0_5 RBL0_13 WBLb_2 RBL1_25 WBLb_25 WBLb_17 RBL1_17 WBLb_9 RBL1_1 WBLb_1 RBL1_9 WBLb_24 WBLb_16 RBL1_23
+ RBL1_31 WBLb_0 WBLb_8 RBL1_7 RBL1_15 WBL_29 WBL_21 RBL0_17 RBL0_25 WBL_5 RBL0_1 WBL_13 RBL0_9 RBL0_28
+ WBLb_28 WBLb_20 RBL0_20 WBLb_12 WBLb_4 RBL0_4 RBL0_12 RBL0_27 WBL_30 WBL_22 RBL0_19 WBL_14 RBL0_11 WBL_6
+ RBL0_3 RBL1_24 WBLb_27 WBLb_19 RBL1_16 WBLb_11 RBL1_8 WBLb_3 RBL1_0 RBL0_24 WBLb_31 WBLb_23 RBL0_16 RBL0_8
+ WBLb_15 RBL0_0 WBLb_7 WWL_17 RWL_17 VDD GND 10T_1x32_xschem
x17 RBL0_22 WBL_25 RBL0_30 WBL_17 WBL_9 WBL_1 RBL0_14 RBL0_6 WBL_18 RBL0_18 RBL0_26 WBL_26 WBL_2
+ RBL0_2 RBL0_10 WBL_10 WBL_19 WBL_27 RBL1_30 RBL1_22 RBL1_14 WBL_3 RBL1_6 WBL_11 WBLb_30 WBLb_22 RBL0_31
+ RBL0_23 RBL0_7 RBL0_15 WBLb_6 WBLb_14 RBL1_21 WBL_20 RBL1_29 WBL_28 WBL_12 RBL1_13 RBL1_5 WBL_4 RBL1_20
+ WBL_23 WBL_31 RBL1_28 WBL_15 RBL1_4 RBL1_12 WBL_7 WBLb_29 WBLb_21 RBL1_19 RBL1_27 RBL1_3 WBLb_5 WBLb_13
+ RBL1_11 WBL_24 WBL_16 RBL1_18 RBL1_26 WBL_8 RBL1_2 RBL1_10 WBL_0 WBLb_26 RBL0_29 WBLb_18 RBL0_21 WBLb_10
+ RBL0_5 RBL0_13 WBLb_2 RBL1_25 WBLb_25 WBLb_17 RBL1_17 WBLb_9 RBL1_1 WBLb_1 RBL1_9 WBLb_24 WBLb_16 RBL1_23
+ RBL1_31 WBLb_0 WBLb_8 RBL1_7 RBL1_15 WBL_29 WBL_21 RBL0_17 RBL0_25 WBL_5 RBL0_1 WBL_13 RBL0_9 RBL0_28
+ WBLb_28 WBLb_20 RBL0_20 WBLb_12 WBLb_4 RBL0_4 RBL0_12 RBL0_27 WBL_30 WBL_22 RBL0_19 WBL_14 RBL0_11 WBL_6
+ RBL0_3 RBL1_24 WBLb_27 WBLb_19 RBL1_16 WBLb_11 RBL1_8 WBLb_3 RBL1_0 RBL0_24 WBLb_31 WBLb_23 RBL0_16 RBL0_8
+ WBLb_15 RBL0_0 WBLb_7 WWL_11 RWL_11 VDD GND 10T_1x32_xschem
x18 RBL0_22 WBL_25 RBL0_30 WBL_17 WBL_9 WBL_1 RBL0_14 RBL0_6 WBL_18 RBL0_18 RBL0_26 WBL_26 WBL_2
+ RBL0_2 RBL0_10 WBL_10 WBL_19 WBL_27 RBL1_30 RBL1_22 RBL1_14 WBL_3 RBL1_6 WBL_11 WBLb_30 WBLb_22 RBL0_31
+ RBL0_23 RBL0_7 RBL0_15 WBLb_6 WBLb_14 RBL1_21 WBL_20 RBL1_29 WBL_28 WBL_12 RBL1_13 RBL1_5 WBL_4 RBL1_20
+ WBL_23 WBL_31 RBL1_28 WBL_15 RBL1_4 RBL1_12 WBL_7 WBLb_29 WBLb_21 RBL1_19 RBL1_27 RBL1_3 WBLb_5 WBLb_13
+ RBL1_11 WBL_24 WBL_16 RBL1_18 RBL1_26 WBL_8 RBL1_2 RBL1_10 WBL_0 WBLb_26 RBL0_29 WBLb_18 RBL0_21 WBLb_10
+ RBL0_5 RBL0_13 WBLb_2 RBL1_25 WBLb_25 WBLb_17 RBL1_17 WBLb_9 RBL1_1 WBLb_1 RBL1_9 WBLb_24 WBLb_16 RBL1_23
+ RBL1_31 WBLb_0 WBLb_8 RBL1_7 RBL1_15 WBL_29 WBL_21 RBL0_17 RBL0_25 WBL_5 RBL0_1 WBL_13 RBL0_9 RBL0_28
+ WBLb_28 WBLb_20 RBL0_20 WBLb_12 WBLb_4 RBL0_4 RBL0_12 RBL0_27 WBL_30 WBL_22 RBL0_19 WBL_14 RBL0_11 WBL_6
+ RBL0_3 RBL1_24 WBLb_27 WBLb_19 RBL1_16 WBLb_11 RBL1_8 WBLb_3 RBL1_0 RBL0_24 WBLb_31 WBLb_23 RBL0_16 RBL0_8
+ WBLb_15 RBL0_0 WBLb_7 WWL_10 RWL_10 VDD GND 10T_1x32_xschem
x19 RBL0_22 WBL_25 RBL0_30 WBL_17 WBL_9 WBL_1 RBL0_14 RBL0_6 WBL_18 RBL0_18 RBL0_26 WBL_26 WBL_2
+ RBL0_2 RBL0_10 WBL_10 WBL_19 WBL_27 RBL1_30 RBL1_22 RBL1_14 WBL_3 RBL1_6 WBL_11 WBLb_30 WBLb_22 RBL0_31
+ RBL0_23 RBL0_7 RBL0_15 WBLb_6 WBLb_14 RBL1_21 WBL_20 RBL1_29 WBL_28 WBL_12 RBL1_13 RBL1_5 WBL_4 RBL1_20
+ WBL_23 WBL_31 RBL1_28 WBL_15 RBL1_4 RBL1_12 WBL_7 WBLb_29 WBLb_21 RBL1_19 RBL1_27 RBL1_3 WBLb_5 WBLb_13
+ RBL1_11 WBL_24 WBL_16 RBL1_18 RBL1_26 WBL_8 RBL1_2 RBL1_10 WBL_0 WBLb_26 RBL0_29 WBLb_18 RBL0_21 WBLb_10
+ RBL0_5 RBL0_13 WBLb_2 RBL1_25 WBLb_25 WBLb_17 RBL1_17 WBLb_9 RBL1_1 WBLb_1 RBL1_9 WBLb_24 WBLb_16 RBL1_23
+ RBL1_31 WBLb_0 WBLb_8 RBL1_7 RBL1_15 WBL_29 WBL_21 RBL0_17 RBL0_25 WBL_5 RBL0_1 WBL_13 RBL0_9 RBL0_28
+ WBLb_28 WBLb_20 RBL0_20 WBLb_12 WBLb_4 RBL0_4 RBL0_12 RBL0_27 WBL_30 WBL_22 RBL0_19 WBL_14 RBL0_11 WBL_6
+ RBL0_3 RBL1_24 WBLb_27 WBLb_19 RBL1_16 WBLb_11 RBL1_8 WBLb_3 RBL1_0 RBL0_24 WBLb_31 WBLb_23 RBL0_16 RBL0_8
+ WBLb_15 RBL0_0 WBLb_7 WWL_18 RWL_18 VDD GND 10T_1x32_xschem
x20 RBL0_22 WBL_25 RBL0_30 WBL_17 WBL_9 WBL_1 RBL0_14 RBL0_6 WBL_18 RBL0_18 RBL0_26 WBL_26 WBL_2
+ RBL0_2 RBL0_10 WBL_10 WBL_19 WBL_27 RBL1_30 RBL1_22 RBL1_14 WBL_3 RBL1_6 WBL_11 WBLb_30 WBLb_22 RBL0_31
+ RBL0_23 RBL0_7 RBL0_15 WBLb_6 WBLb_14 RBL1_21 WBL_20 RBL1_29 WBL_28 WBL_12 RBL1_13 RBL1_5 WBL_4 RBL1_20
+ WBL_23 WBL_31 RBL1_28 WBL_15 RBL1_4 RBL1_12 WBL_7 WBLb_29 WBLb_21 RBL1_19 RBL1_27 RBL1_3 WBLb_5 WBLb_13
+ RBL1_11 WBL_24 WBL_16 RBL1_18 RBL1_26 WBL_8 RBL1_2 RBL1_10 WBL_0 WBLb_26 RBL0_29 WBLb_18 RBL0_21 WBLb_10
+ RBL0_5 RBL0_13 WBLb_2 RBL1_25 WBLb_25 WBLb_17 RBL1_17 WBLb_9 RBL1_1 WBLb_1 RBL1_9 WBLb_24 WBLb_16 RBL1_23
+ RBL1_31 WBLb_0 WBLb_8 RBL1_7 RBL1_15 WBL_29 WBL_21 RBL0_17 RBL0_25 WBL_5 RBL0_1 WBL_13 RBL0_9 RBL0_28
+ WBLb_28 WBLb_20 RBL0_20 WBLb_12 WBLb_4 RBL0_4 RBL0_12 RBL0_27 WBL_30 WBL_22 RBL0_19 WBL_14 RBL0_11 WBL_6
+ RBL0_3 RBL1_24 WBLb_27 WBLb_19 RBL1_16 WBLb_11 RBL1_8 WBLb_3 RBL1_0 RBL0_24 WBLb_31 WBLb_23 RBL0_16 RBL0_8
+ WBLb_15 RBL0_0 WBLb_7 WWL_19 RWL_19 VDD GND 10T_1x32_xschem
x21 RBL0_22 WBL_25 RBL0_30 WBL_17 WBL_9 WBL_1 RBL0_14 RBL0_6 WBL_18 RBL0_18 RBL0_26 WBL_26 WBL_2
+ RBL0_2 RBL0_10 WBL_10 WBL_19 WBL_27 RBL1_30 RBL1_22 RBL1_14 WBL_3 RBL1_6 WBL_11 WBLb_30 WBLb_22 RBL0_31
+ RBL0_23 RBL0_7 RBL0_15 WBLb_6 WBLb_14 RBL1_21 WBL_20 RBL1_29 WBL_28 WBL_12 RBL1_13 RBL1_5 WBL_4 RBL1_20
+ WBL_23 WBL_31 RBL1_28 WBL_15 RBL1_4 RBL1_12 WBL_7 WBLb_29 WBLb_21 RBL1_19 RBL1_27 RBL1_3 WBLb_5 WBLb_13
+ RBL1_11 WBL_24 WBL_16 RBL1_18 RBL1_26 WBL_8 RBL1_2 RBL1_10 WBL_0 WBLb_26 RBL0_29 WBLb_18 RBL0_21 WBLb_10
+ RBL0_5 RBL0_13 WBLb_2 RBL1_25 WBLb_25 WBLb_17 RBL1_17 WBLb_9 RBL1_1 WBLb_1 RBL1_9 WBLb_24 WBLb_16 RBL1_23
+ RBL1_31 WBLb_0 WBLb_8 RBL1_7 RBL1_15 WBL_29 WBL_21 RBL0_17 RBL0_25 WBL_5 RBL0_1 WBL_13 RBL0_9 RBL0_28
+ WBLb_28 WBLb_20 RBL0_20 WBLb_12 WBLb_4 RBL0_4 RBL0_12 RBL0_27 WBL_30 WBL_22 RBL0_19 WBL_14 RBL0_11 WBL_6
+ RBL0_3 RBL1_24 WBLb_27 WBLb_19 RBL1_16 WBLb_11 RBL1_8 WBLb_3 RBL1_0 RBL0_24 WBLb_31 WBLb_23 RBL0_16 RBL0_8
+ WBLb_15 RBL0_0 WBLb_7 WWL_22 RWL_22 VDD GND 10T_1x32_xschem
x22 RBL0_22 WBL_25 RBL0_30 WBL_17 WBL_9 WBL_1 RBL0_14 RBL0_6 WBL_18 RBL0_18 RBL0_26 WBL_26 WBL_2
+ RBL0_2 RBL0_10 WBL_10 WBL_19 WBL_27 RBL1_30 RBL1_22 RBL1_14 WBL_3 RBL1_6 WBL_11 WBLb_30 WBLb_22 RBL0_31
+ RBL0_23 RBL0_7 RBL0_15 WBLb_6 WBLb_14 RBL1_21 WBL_20 RBL1_29 WBL_28 WBL_12 RBL1_13 RBL1_5 WBL_4 RBL1_20
+ WBL_23 WBL_31 RBL1_28 WBL_15 RBL1_4 RBL1_12 WBL_7 WBLb_29 WBLb_21 RBL1_19 RBL1_27 RBL1_3 WBLb_5 WBLb_13
+ RBL1_11 WBL_24 WBL_16 RBL1_18 RBL1_26 WBL_8 RBL1_2 RBL1_10 WBL_0 WBLb_26 RBL0_29 WBLb_18 RBL0_21 WBLb_10
+ RBL0_5 RBL0_13 WBLb_2 RBL1_25 WBLb_25 WBLb_17 RBL1_17 WBLb_9 RBL1_1 WBLb_1 RBL1_9 WBLb_24 WBLb_16 RBL1_23
+ RBL1_31 WBLb_0 WBLb_8 RBL1_7 RBL1_15 WBL_29 WBL_21 RBL0_17 RBL0_25 WBL_5 RBL0_1 WBL_13 RBL0_9 RBL0_28
+ WBLb_28 WBLb_20 RBL0_20 WBLb_12 WBLb_4 RBL0_4 RBL0_12 RBL0_27 WBL_30 WBL_22 RBL0_19 WBL_14 RBL0_11 WBL_6
+ RBL0_3 RBL1_24 WBLb_27 WBLb_19 RBL1_16 WBLb_11 RBL1_8 WBLb_3 RBL1_0 RBL0_24 WBLb_31 WBLb_23 RBL0_16 RBL0_8
+ WBLb_15 RBL0_0 WBLb_7 WWL_23 RWL_23 VDD GND 10T_1x32_xschem
x23 RBL0_22 WBL_25 RBL0_30 WBL_17 WBL_9 WBL_1 RBL0_14 RBL0_6 WBL_18 RBL0_18 RBL0_26 WBL_26 WBL_2
+ RBL0_2 RBL0_10 WBL_10 WBL_19 WBL_27 RBL1_30 RBL1_22 RBL1_14 WBL_3 RBL1_6 WBL_11 WBLb_30 WBLb_22 RBL0_31
+ RBL0_23 RBL0_7 RBL0_15 WBLb_6 WBLb_14 RBL1_21 WBL_20 RBL1_29 WBL_28 WBL_12 RBL1_13 RBL1_5 WBL_4 RBL1_20
+ WBL_23 WBL_31 RBL1_28 WBL_15 RBL1_4 RBL1_12 WBL_7 WBLb_29 WBLb_21 RBL1_19 RBL1_27 RBL1_3 WBLb_5 WBLb_13
+ RBL1_11 WBL_24 WBL_16 RBL1_18 RBL1_26 WBL_8 RBL1_2 RBL1_10 WBL_0 WBLb_26 RBL0_29 WBLb_18 RBL0_21 WBLb_10
+ RBL0_5 RBL0_13 WBLb_2 RBL1_25 WBLb_25 WBLb_17 RBL1_17 WBLb_9 RBL1_1 WBLb_1 RBL1_9 WBLb_24 WBLb_16 RBL1_23
+ RBL1_31 WBLb_0 WBLb_8 RBL1_7 RBL1_15 WBL_29 WBL_21 RBL0_17 RBL0_25 WBL_5 RBL0_1 WBL_13 RBL0_9 RBL0_28
+ WBLb_28 WBLb_20 RBL0_20 WBLb_12 WBLb_4 RBL0_4 RBL0_12 RBL0_27 WBL_30 WBL_22 RBL0_19 WBL_14 RBL0_11 WBL_6
+ RBL0_3 RBL1_24 WBLb_27 WBLb_19 RBL1_16 WBLb_11 RBL1_8 WBLb_3 RBL1_0 RBL0_24 WBLb_31 WBLb_23 RBL0_16 RBL0_8
+ WBLb_15 RBL0_0 WBLb_7 WWL_24 RWL_24 VDD GND 10T_1x32_xschem
x24 RBL0_22 WBL_25 RBL0_30 WBL_17 WBL_9 WBL_1 RBL0_14 RBL0_6 WBL_18 RBL0_18 RBL0_26 WBL_26 WBL_2
+ RBL0_2 RBL0_10 WBL_10 WBL_19 WBL_27 RBL1_30 RBL1_22 RBL1_14 WBL_3 RBL1_6 WBL_11 WBLb_30 WBLb_22 RBL0_31
+ RBL0_23 RBL0_7 RBL0_15 WBLb_6 WBLb_14 RBL1_21 WBL_20 RBL1_29 WBL_28 WBL_12 RBL1_13 RBL1_5 WBL_4 RBL1_20
+ WBL_23 WBL_31 RBL1_28 WBL_15 RBL1_4 RBL1_12 WBL_7 WBLb_29 WBLb_21 RBL1_19 RBL1_27 RBL1_3 WBLb_5 WBLb_13
+ RBL1_11 WBL_24 WBL_16 RBL1_18 RBL1_26 WBL_8 RBL1_2 RBL1_10 WBL_0 WBLb_26 RBL0_29 WBLb_18 RBL0_21 WBLb_10
+ RBL0_5 RBL0_13 WBLb_2 RBL1_25 WBLb_25 WBLb_17 RBL1_17 WBLb_9 RBL1_1 WBLb_1 RBL1_9 WBLb_24 WBLb_16 RBL1_23
+ RBL1_31 WBLb_0 WBLb_8 RBL1_7 RBL1_15 WBL_29 WBL_21 RBL0_17 RBL0_25 WBL_5 RBL0_1 WBL_13 RBL0_9 RBL0_28
+ WBLb_28 WBLb_20 RBL0_20 WBLb_12 WBLb_4 RBL0_4 RBL0_12 RBL0_27 WBL_30 WBL_22 RBL0_19 WBL_14 RBL0_11 WBL_6
+ RBL0_3 RBL1_24 WBLb_27 WBLb_19 RBL1_16 WBLb_11 RBL1_8 WBLb_3 RBL1_0 RBL0_24 WBLb_31 WBLb_23 RBL0_16 RBL0_8
+ WBLb_15 RBL0_0 WBLb_7 WWL_25 RWL_25 VDD GND 10T_1x32_xschem
x25 RBL0_22 WBL_25 RBL0_30 WBL_17 WBL_9 WBL_1 RBL0_14 RBL0_6 WBL_18 RBL0_18 RBL0_26 WBL_26 WBL_2
+ RBL0_2 RBL0_10 WBL_10 WBL_19 WBL_27 RBL1_30 RBL1_22 RBL1_14 WBL_3 RBL1_6 WBL_11 WBLb_30 WBLb_22 RBL0_31
+ RBL0_23 RBL0_7 RBL0_15 WBLb_6 WBLb_14 RBL1_21 WBL_20 RBL1_29 WBL_28 WBL_12 RBL1_13 RBL1_5 WBL_4 RBL1_20
+ WBL_23 WBL_31 RBL1_28 WBL_15 RBL1_4 RBL1_12 WBL_7 WBLb_29 WBLb_21 RBL1_19 RBL1_27 RBL1_3 WBLb_5 WBLb_13
+ RBL1_11 WBL_24 WBL_16 RBL1_18 RBL1_26 WBL_8 RBL1_2 RBL1_10 WBL_0 WBLb_26 RBL0_29 WBLb_18 RBL0_21 WBLb_10
+ RBL0_5 RBL0_13 WBLb_2 RBL1_25 WBLb_25 WBLb_17 RBL1_17 WBLb_9 RBL1_1 WBLb_1 RBL1_9 WBLb_24 WBLb_16 RBL1_23
+ RBL1_31 WBLb_0 WBLb_8 RBL1_7 RBL1_15 WBL_29 WBL_21 RBL0_17 RBL0_25 WBL_5 RBL0_1 WBL_13 RBL0_9 RBL0_28
+ WBLb_28 WBLb_20 RBL0_20 WBLb_12 WBLb_4 RBL0_4 RBL0_12 RBL0_27 WBL_30 WBL_22 RBL0_19 WBL_14 RBL0_11 WBL_6
+ RBL0_3 RBL1_24 WBLb_27 WBLb_19 RBL1_16 WBLb_11 RBL1_8 WBLb_3 RBL1_0 RBL0_24 WBLb_31 WBLb_23 RBL0_16 RBL0_8
+ WBLb_15 RBL0_0 WBLb_7 WWL_26 RWL_26 VDD GND 10T_1x32_xschem
x26 RBL0_22 WBL_25 RBL0_30 WBL_17 WBL_9 WBL_1 RBL0_14 RBL0_6 WBL_18 RBL0_18 RBL0_26 WBL_26 WBL_2
+ RBL0_2 RBL0_10 WBL_10 WBL_19 WBL_27 RBL1_30 RBL1_22 RBL1_14 WBL_3 RBL1_6 WBL_11 WBLb_30 WBLb_22 RBL0_31
+ RBL0_23 RBL0_7 RBL0_15 WBLb_6 WBLb_14 RBL1_21 WBL_20 RBL1_29 WBL_28 WBL_12 RBL1_13 RBL1_5 WBL_4 RBL1_20
+ WBL_23 WBL_31 RBL1_28 WBL_15 RBL1_4 RBL1_12 WBL_7 WBLb_29 WBLb_21 RBL1_19 RBL1_27 RBL1_3 WBLb_5 WBLb_13
+ RBL1_11 WBL_24 WBL_16 RBL1_18 RBL1_26 WBL_8 RBL1_2 RBL1_10 WBL_0 WBLb_26 RBL0_29 WBLb_18 RBL0_21 WBLb_10
+ RBL0_5 RBL0_13 WBLb_2 RBL1_25 WBLb_25 WBLb_17 RBL1_17 WBLb_9 RBL1_1 WBLb_1 RBL1_9 WBLb_24 WBLb_16 RBL1_23
+ RBL1_31 WBLb_0 WBLb_8 RBL1_7 RBL1_15 WBL_29 WBL_21 RBL0_17 RBL0_25 WBL_5 RBL0_1 WBL_13 RBL0_9 RBL0_28
+ WBLb_28 WBLb_20 RBL0_20 WBLb_12 WBLb_4 RBL0_4 RBL0_12 RBL0_27 WBL_30 WBL_22 RBL0_19 WBL_14 RBL0_11 WBL_6
+ RBL0_3 RBL1_24 WBLb_27 WBLb_19 RBL1_16 WBLb_11 RBL1_8 WBLb_3 RBL1_0 RBL0_24 WBLb_31 WBLb_23 RBL0_16 RBL0_8
+ WBLb_15 RBL0_0 WBLb_7 WWL_27 RWL_27 VDD GND 10T_1x32_xschem
x27 RBL0_22 WBL_25 RBL0_30 WBL_17 WBL_9 WBL_1 RBL0_14 RBL0_6 WBL_18 RBL0_18 RBL0_26 WBL_26 WBL_2
+ RBL0_2 RBL0_10 WBL_10 WBL_19 WBL_27 RBL1_30 RBL1_22 RBL1_14 WBL_3 RBL1_6 WBL_11 WBLb_30 WBLb_22 RBL0_31
+ RBL0_23 RBL0_7 RBL0_15 WBLb_6 WBLb_14 RBL1_21 WBL_20 RBL1_29 WBL_28 WBL_12 RBL1_13 RBL1_5 WBL_4 RBL1_20
+ WBL_23 WBL_31 RBL1_28 WBL_15 RBL1_4 RBL1_12 WBL_7 WBLb_29 WBLb_21 RBL1_19 RBL1_27 RBL1_3 WBLb_5 WBLb_13
+ RBL1_11 WBL_24 WBL_16 RBL1_18 RBL1_26 WBL_8 RBL1_2 RBL1_10 WBL_0 WBLb_26 RBL0_29 WBLb_18 RBL0_21 WBLb_10
+ RBL0_5 RBL0_13 WBLb_2 RBL1_25 WBLb_25 WBLb_17 RBL1_17 WBLb_9 RBL1_1 WBLb_1 RBL1_9 WBLb_24 WBLb_16 RBL1_23
+ RBL1_31 WBLb_0 WBLb_8 RBL1_7 RBL1_15 WBL_29 WBL_21 RBL0_17 RBL0_25 WBL_5 RBL0_1 WBL_13 RBL0_9 RBL0_28
+ WBLb_28 WBLb_20 RBL0_20 WBLb_12 WBLb_4 RBL0_4 RBL0_12 RBL0_27 WBL_30 WBL_22 RBL0_19 WBL_14 RBL0_11 WBL_6
+ RBL0_3 RBL1_24 WBLb_27 WBLb_19 RBL1_16 WBLb_11 RBL1_8 WBLb_3 RBL1_0 RBL0_24 WBLb_31 WBLb_23 RBL0_16 RBL0_8
+ WBLb_15 RBL0_0 WBLb_7 WWL_21 RWL_21 VDD GND 10T_1x32_xschem
x28 RBL0_22 WBL_25 RBL0_30 WBL_17 WBL_9 WBL_1 RBL0_14 RBL0_6 WBL_18 RBL0_18 RBL0_26 WBL_26 WBL_2
+ RBL0_2 RBL0_10 WBL_10 WBL_19 WBL_27 RBL1_30 RBL1_22 RBL1_14 WBL_3 RBL1_6 WBL_11 WBLb_30 WBLb_22 RBL0_31
+ RBL0_23 RBL0_7 RBL0_15 WBLb_6 WBLb_14 RBL1_21 WBL_20 RBL1_29 WBL_28 WBL_12 RBL1_13 RBL1_5 WBL_4 RBL1_20
+ WBL_23 WBL_31 RBL1_28 WBL_15 RBL1_4 RBL1_12 WBL_7 WBLb_29 WBLb_21 RBL1_19 RBL1_27 RBL1_3 WBLb_5 WBLb_13
+ RBL1_11 WBL_24 WBL_16 RBL1_18 RBL1_26 WBL_8 RBL1_2 RBL1_10 WBL_0 WBLb_26 RBL0_29 WBLb_18 RBL0_21 WBLb_10
+ RBL0_5 RBL0_13 WBLb_2 RBL1_25 WBLb_25 WBLb_17 RBL1_17 WBLb_9 RBL1_1 WBLb_1 RBL1_9 WBLb_24 WBLb_16 RBL1_23
+ RBL1_31 WBLb_0 WBLb_8 RBL1_7 RBL1_15 WBL_29 WBL_21 RBL0_17 RBL0_25 WBL_5 RBL0_1 WBL_13 RBL0_9 RBL0_28
+ WBLb_28 WBLb_20 RBL0_20 WBLb_12 WBLb_4 RBL0_4 RBL0_12 RBL0_27 WBL_30 WBL_22 RBL0_19 WBL_14 RBL0_11 WBL_6
+ RBL0_3 RBL1_24 WBLb_27 WBLb_19 RBL1_16 WBLb_11 RBL1_8 WBLb_3 RBL1_0 RBL0_24 WBLb_31 WBLb_23 RBL0_16 RBL0_8
+ WBLb_15 RBL0_0 WBLb_7 WWL_20 RWL_20 VDD GND 10T_1x32_xschem
x29 RBL0_22 WBL_25 RBL0_30 WBL_17 WBL_9 WBL_1 RBL0_14 RBL0_6 WBL_18 RBL0_18 RBL0_26 WBL_26 WBL_2
+ RBL0_2 RBL0_10 WBL_10 WBL_19 WBL_27 RBL1_30 RBL1_22 RBL1_14 WBL_3 RBL1_6 WBL_11 WBLb_30 WBLb_22 RBL0_31
+ RBL0_23 RBL0_7 RBL0_15 WBLb_6 WBLb_14 RBL1_21 WBL_20 RBL1_29 WBL_28 WBL_12 RBL1_13 RBL1_5 WBL_4 RBL1_20
+ WBL_23 WBL_31 RBL1_28 WBL_15 RBL1_4 RBL1_12 WBL_7 WBLb_29 WBLb_21 RBL1_19 RBL1_27 RBL1_3 WBLb_5 WBLb_13
+ RBL1_11 WBL_24 WBL_16 RBL1_18 RBL1_26 WBL_8 RBL1_2 RBL1_10 WBL_0 WBLb_26 RBL0_29 WBLb_18 RBL0_21 WBLb_10
+ RBL0_5 RBL0_13 WBLb_2 RBL1_25 WBLb_25 WBLb_17 RBL1_17 WBLb_9 RBL1_1 WBLb_1 RBL1_9 WBLb_24 WBLb_16 RBL1_23
+ RBL1_31 WBLb_0 WBLb_8 RBL1_7 RBL1_15 WBL_29 WBL_21 RBL0_17 RBL0_25 WBL_5 RBL0_1 WBL_13 RBL0_9 RBL0_28
+ WBLb_28 WBLb_20 RBL0_20 WBLb_12 WBLb_4 RBL0_4 RBL0_12 RBL0_27 WBL_30 WBL_22 RBL0_19 WBL_14 RBL0_11 WBL_6
+ RBL0_3 RBL1_24 WBLb_27 WBLb_19 RBL1_16 WBLb_11 RBL1_8 WBLb_3 RBL1_0 RBL0_24 WBLb_31 WBLb_23 RBL0_16 RBL0_8
+ WBLb_15 RBL0_0 WBLb_7 WWL_28 RWL_28 VDD GND 10T_1x32_xschem
x30 RBL0_22 WBL_25 RBL0_30 WBL_17 WBL_9 WBL_1 RBL0_14 RBL0_6 WBL_18 RBL0_18 RBL0_26 WBL_26 WBL_2
+ RBL0_2 RBL0_10 WBL_10 WBL_19 WBL_27 RBL1_30 RBL1_22 RBL1_14 WBL_3 RBL1_6 WBL_11 WBLb_30 WBLb_22 RBL0_31
+ RBL0_23 RBL0_7 RBL0_15 WBLb_6 WBLb_14 RBL1_21 WBL_20 RBL1_29 WBL_28 WBL_12 RBL1_13 RBL1_5 WBL_4 RBL1_20
+ WBL_23 WBL_31 RBL1_28 WBL_15 RBL1_4 RBL1_12 WBL_7 WBLb_29 WBLb_21 RBL1_19 RBL1_27 RBL1_3 WBLb_5 WBLb_13
+ RBL1_11 WBL_24 WBL_16 RBL1_18 RBL1_26 WBL_8 RBL1_2 RBL1_10 WBL_0 WBLb_26 RBL0_29 WBLb_18 RBL0_21 WBLb_10
+ RBL0_5 RBL0_13 WBLb_2 RBL1_25 WBLb_25 WBLb_17 RBL1_17 WBLb_9 RBL1_1 WBLb_1 RBL1_9 WBLb_24 WBLb_16 RBL1_23
+ RBL1_31 WBLb_0 WBLb_8 RBL1_7 RBL1_15 WBL_29 WBL_21 RBL0_17 RBL0_25 WBL_5 RBL0_1 WBL_13 RBL0_9 RBL0_28
+ WBLb_28 WBLb_20 RBL0_20 WBLb_12 WBLb_4 RBL0_4 RBL0_12 RBL0_27 WBL_30 WBL_22 RBL0_19 WBL_14 RBL0_11 WBL_6
+ RBL0_3 RBL1_24 WBLb_27 WBLb_19 RBL1_16 WBLb_11 RBL1_8 WBLb_3 RBL1_0 RBL0_24 WBLb_31 WBLb_23 RBL0_16 RBL0_8
+ WBLb_15 RBL0_0 WBLb_7 WWL_29 RWL_29 VDD GND 10T_1x32_xschem
x31 RBL0_22 WBL_25 RBL0_30 WBL_17 WBL_9 WBL_1 RBL0_14 RBL0_6 WBL_18 RBL0_18 RBL0_26 WBL_26 WBL_2
+ RBL0_2 RBL0_10 WBL_10 WBL_19 WBL_27 RBL1_30 RBL1_22 RBL1_14 WBL_3 RBL1_6 WBL_11 WBLb_30 WBLb_22 RBL0_31
+ RBL0_23 RBL0_7 RBL0_15 WBLb_6 WBLb_14 RBL1_21 WBL_20 RBL1_29 WBL_28 WBL_12 RBL1_13 RBL1_5 WBL_4 RBL1_20
+ WBL_23 WBL_31 RBL1_28 WBL_15 RBL1_4 RBL1_12 WBL_7 WBLb_29 WBLb_21 RBL1_19 RBL1_27 RBL1_3 WBLb_5 WBLb_13
+ RBL1_11 WBL_24 WBL_16 RBL1_18 RBL1_26 WBL_8 RBL1_2 RBL1_10 WBL_0 WBLb_26 RBL0_29 WBLb_18 RBL0_21 WBLb_10
+ RBL0_5 RBL0_13 WBLb_2 RBL1_25 WBLb_25 WBLb_17 RBL1_17 WBLb_9 RBL1_1 WBLb_1 RBL1_9 WBLb_24 WBLb_16 RBL1_23
+ RBL1_31 WBLb_0 WBLb_8 RBL1_7 RBL1_15 WBL_29 WBL_21 RBL0_17 RBL0_25 WBL_5 RBL0_1 WBL_13 RBL0_9 RBL0_28
+ WBLb_28 WBLb_20 RBL0_20 WBLb_12 WBLb_4 RBL0_4 RBL0_12 RBL0_27 WBL_30 WBL_22 RBL0_19 WBL_14 RBL0_11 WBL_6
+ RBL0_3 RBL1_24 WBLb_27 WBLb_19 RBL1_16 WBLb_11 RBL1_8 WBLb_3 RBL1_0 RBL0_24 WBLb_31 WBLb_23 RBL0_16 RBL0_8
+ WBLb_15 RBL0_0 WBLb_7 WWL_30 RWL_30 VDD GND 10T_1x32_xschem
x32 RBL0_22 WBL_25 RBL0_30 WBL_17 WBL_9 WBL_1 RBL0_14 RBL0_6 WBL_18 RBL0_18 RBL0_26 WBL_26 WBL_2
+ RBL0_2 RBL0_10 WBL_10 WBL_19 WBL_27 RBL1_30 RBL1_22 RBL1_14 WBL_3 RBL1_6 WBL_11 WBLb_30 WBLb_22 RBL0_31
+ RBL0_23 RBL0_7 RBL0_15 WBLb_6 WBLb_14 RBL1_21 WBL_20 RBL1_29 WBL_28 WBL_12 RBL1_13 RBL1_5 WBL_4 RBL1_20
+ WBL_23 WBL_31 RBL1_28 WBL_15 RBL1_4 RBL1_12 WBL_7 WBLb_29 WBLb_21 RBL1_19 RBL1_27 RBL1_3 WBLb_5 WBLb_13
+ RBL1_11 WBL_24 WBL_16 RBL1_18 RBL1_26 WBL_8 RBL1_2 RBL1_10 WBL_0 WBLb_26 RBL0_29 WBLb_18 RBL0_21 WBLb_10
+ RBL0_5 RBL0_13 WBLb_2 RBL1_25 WBLb_25 WBLb_17 RBL1_17 WBLb_9 RBL1_1 WBLb_1 RBL1_9 WBLb_24 WBLb_16 RBL1_23
+ RBL1_31 WBLb_0 WBLb_8 RBL1_7 RBL1_15 WBL_29 WBL_21 RBL0_17 RBL0_25 WBL_5 RBL0_1 WBL_13 RBL0_9 RBL0_28
+ WBLb_28 WBLb_20 RBL0_20 WBLb_12 WBLb_4 RBL0_4 RBL0_12 RBL0_27 WBL_30 WBL_22 RBL0_19 WBL_14 RBL0_11 WBL_6
+ RBL0_3 RBL1_24 WBLb_27 WBLb_19 RBL1_16 WBLb_11 RBL1_8 WBLb_3 RBL1_0 RBL0_24 WBLb_31 WBLb_23 RBL0_16 RBL0_8
+ WBLb_15 RBL0_0 WBLb_7 WWL_31 RWL_31 VDD GND 10T_1x32_xschem
**.ends
.end
